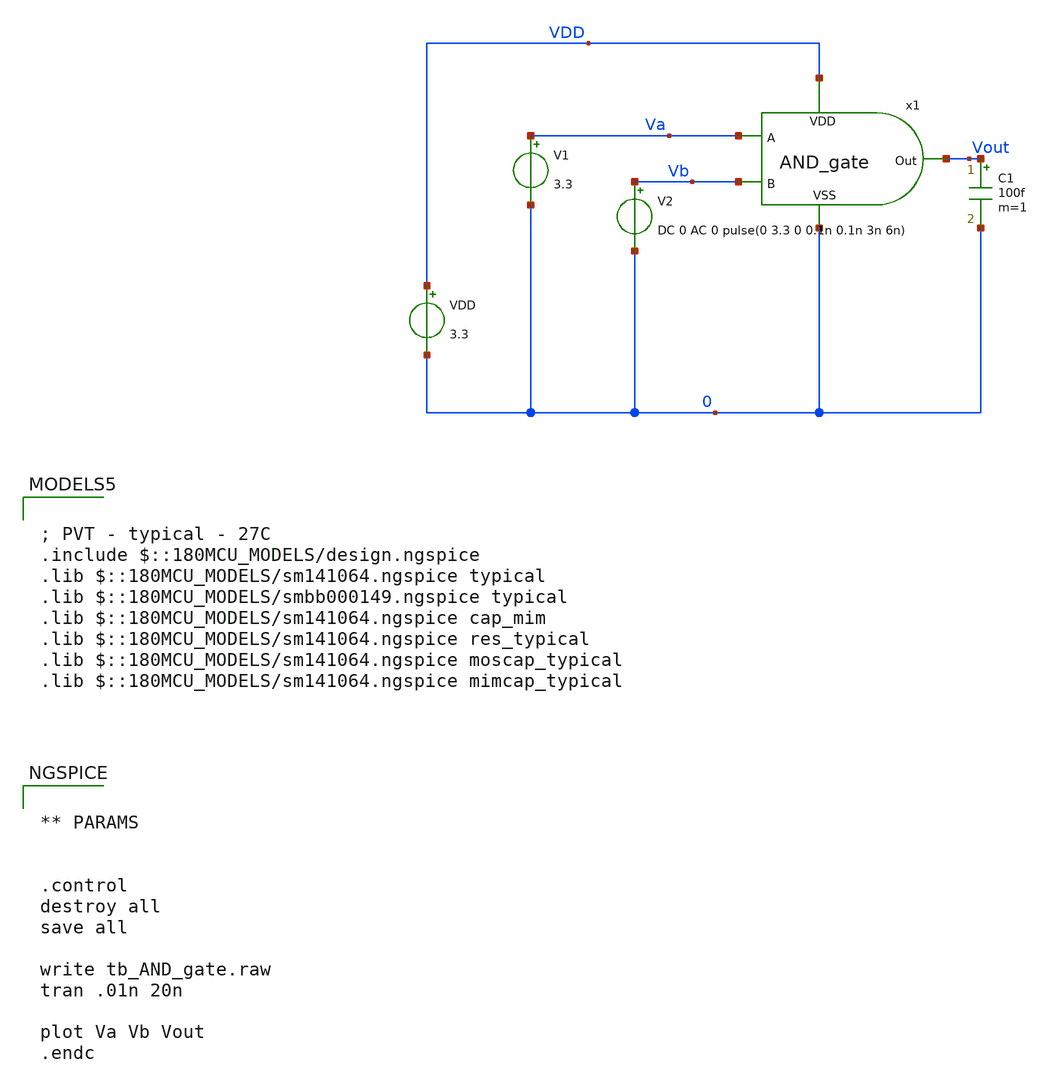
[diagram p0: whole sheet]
** sch_path: designs/digital/testbench/tb_AND_gate.sch
**.subckt tb_AND_gate
VDD VDD 0 3.3
x1 Vout VDD 0 Va Vb AND_gate
C1 Vout 0 100f m=1
V1 Va 0 3.3
V2 Vb 0 DC 0 AC 0 pulse(0 3.3 0 0.1n 0.1n 3n 6n)
**** begin user architecture code

; PVT - typical - 27C
.include $::180MCU_MODELS/design.ngspice
.lib $::180MCU_MODELS/sm141064.ngspice typical
.lib $::180MCU_MODELS/smbb000149.ngspice typical
.lib $::180MCU_MODELS/sm141064.ngspice cap_mim
.lib $::180MCU_MODELS/sm141064.ngspice res_typical
.lib $::180MCU_MODELS/sm141064.ngspice moscap_typical
.lib $::180MCU_MODELS/sm141064.ngspice mimcap_typical



** PARAMS


.control
destroy all
save all

write tb_AND_gate.raw
tran .01n 20n

plot Va Vb Vout
.endc


**** end user architecture code
**.ends

* expanding   symbol:  digital/schematic/AND_gate.sym # of pins=5
** sym_path: designs/digital/schematic/AND_gate.sym
** sch_path: designs/digital/schematic/AND_gate.sch
.subckt AND_gate Out VDD VSS A B
*.ipin VDD
*.ipin VSS
*.ipin A
*.ipin B
*.opin Out
XM1 net1 B net2 VSS nfet_03v3 L=0.28u W=8u nf=2 ad='int((nf+1)/2) * W/nf * 0.18u' as='int((nf+2)/2) * W/nf * 0.18u'
+ pd='2*int((nf+1)/2) * (W/nf + 0.18u)' ps='2*int((nf+2)/2) * (W/nf + 0.18u)' nrd='0.18u / W' nrs='0.18u / W'
+ sa=0 sb=0 sd=0 m=1
XM2 net1 A VDD VDD pfet_03v3 L=0.28u W=4u nf=1 ad='int((nf+1)/2) * W/nf * 0.18u' as='int((nf+2)/2) * W/nf * 0.18u'
+ pd='2*int((nf+1)/2) * (W/nf + 0.18u)' ps='2*int((nf+2)/2) * (W/nf + 0.18u)' nrd='0.18u / W' nrs='0.18u / W'
+ sa=0 sb=0 sd=0 m=1
XM3 net1 B VDD VDD pfet_03v3 L=0.28u W=4u nf=1 ad='int((nf+1)/2) * W/nf * 0.18u' as='int((nf+2)/2) * W/nf * 0.18u'
+ pd='2*int((nf+1)/2) * (W/nf + 0.18u)' ps='2*int((nf+2)/2) * (W/nf + 0.18u)' nrd='0.18u / W' nrs='0.18u / W'
+ sa=0 sb=0 sd=0 m=1
XM4 net2 A VSS VSS nfet_03v3 L=0.28u W=8u nf=2 ad='int((nf+1)/2) * W/nf * 0.18u' as='int((nf+2)/2) * W/nf * 0.18u'
+ pd='2*int((nf+1)/2) * (W/nf + 0.18u)' ps='2*int((nf+2)/2) * (W/nf + 0.18u)' nrd='0.18u / W' nrs='0.18u / W'
+ sa=0 sb=0 sd=0 m=1
XM5 Out net1 VSS VSS nfet_03v3 L=0.28u W=4u nf=1 ad='int((nf+1)/2) * W/nf * 0.18u' as='int((nf+2)/2) * W/nf * 0.18u'
+ pd='2*int((nf+1)/2) * (W/nf + 0.18u)' ps='2*int((nf+2)/2) * (W/nf + 0.18u)' nrd='0.18u / W' nrs='0.18u / W'
+ sa=0 sb=0 sd=0 m=1
XM6 Out net1 VDD VDD pfet_03v3 L=0.28u W=8u nf=2 ad='int((nf+1)/2) * W/nf * 0.18u' as='int((nf+2)/2) * W/nf * 0.18u'
+ pd='2*int((nf+1)/2) * (W/nf + 0.18u)' ps='2*int((nf+2)/2) * (W/nf + 0.18u)' nrd='0.18u / W' nrs='0.18u / W'
+ sa=0 sb=0 sd=0 m=1
.ends

.end
